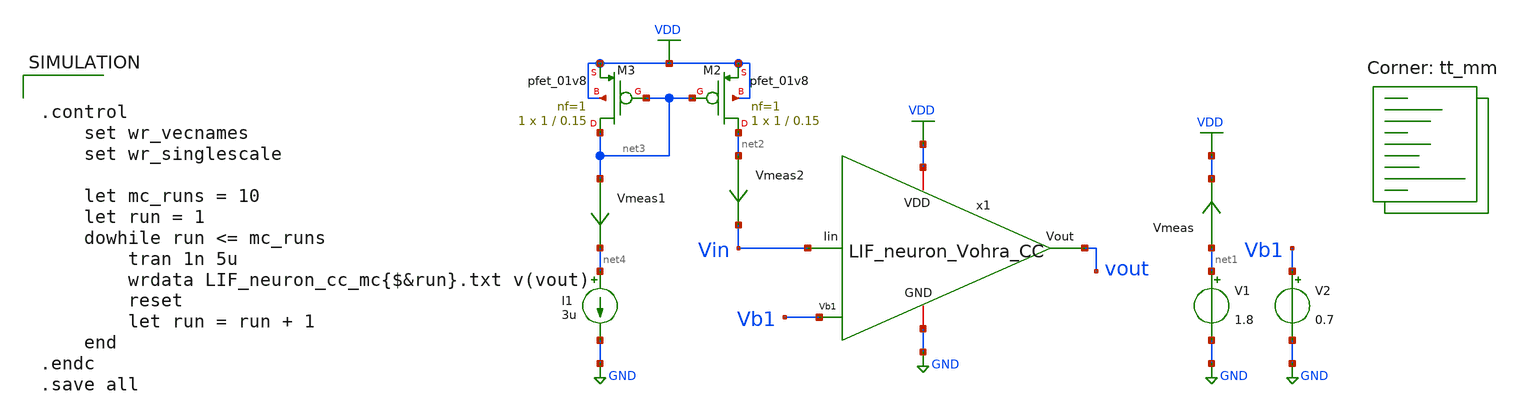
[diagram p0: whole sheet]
** sch_path: LIF_neuron/LIF_neuron_cc_mc.sch
**.subckt LIF_neuron_cc_mc
V1 net1 GND 1.8
V2 Vb1 GND 0.7
x1 VDD vout Vb1 GND Vin LIF_neuron_Vohra_CC
I1 net4 GND 3u
XM2 net2 net3 VDD VDD sky130_fd_pr__pfet_01v8 L=0.15 W=1 nf=1 ad='int((nf+1)/2) * W/nf * 0.29' as='int((nf+2)/2) * W/nf * 0.29'
+ pd='2*int((nf+1)/2) * (W/nf + 0.29)' ps='2*int((nf+2)/2) * (W/nf + 0.29)' nrd='0.29 / W' nrs='0.29 / W'
+ sa=0 sb=0 sd=0 mult=1 m=1
XM3 net3 net3 VDD VDD sky130_fd_pr__pfet_01v8 L=0.15 W=1 nf=1 ad='int((nf+1)/2) * W/nf * 0.29' as='int((nf+2)/2) * W/nf * 0.29'
+ pd='2*int((nf+1)/2) * (W/nf + 0.29)' ps='2*int((nf+2)/2) * (W/nf + 0.29)' nrd='0.29 / W' nrs='0.29 / W'
+ sa=0 sb=0 sd=0 mult=1 m=1
Vmeas net1 VDD 0
.save i(vmeas)
Vmeas1 net3 net4 0
.save i(vmeas1)
Vmeas2 net2 Vin 0
.save i(vmeas2)
**** begin user architecture code


.control
	set wr_vecnames
	set wr_singlescale

	let mc_runs = 10
	let run = 1
	dowhile run <= mc_runs
		tran 1n 5u
		wrdata LIF_neuron_cc_mc{$&run}.txt v(vout)
		reset
		let run = run + 1
	end
.endc
.save all


.lib $::SKYWATER_MODELS/sky130.lib.spice tt_mm
**** end user architecture code
**.ends

* expanding   symbol:  /home/ricardo/RATT_repos/Proyectos_xschem/LIF_neuron/LIF_neuron_Vohra_CC.sym
*+ # of pins=5
** sym_path: LIF_neuron/LIF_neuron_Vohra_CC.sym
** sch_path: LIF_neuron/LIF_neuron_Vohra_CC.sch
.subckt LIF_neuron_Vohra_CC VDD Vout Vb1 GND Iin
*.iopin GND
*.ipin Vb1
*.iopin VDD
*.opin Vout
*.ipin Iin
XM8 net2 Vb1 GND GND sky130_fd_pr__nfet_01v8 L=0.5 W=5 nf=1 ad='int((nf+1)/2) * W/nf * 0.29' as='int((nf+2)/2) * W/nf * 0.29'
+ pd='2*int((nf+1)/2) * (W/nf + 0.29)' ps='2*int((nf+2)/2) * (W/nf + 0.29)' nrd='0.29 / W' nrs='0.29 / W'
+ sa=0 sb=0 sd=0 mult=1 m=1
XM7 rc net1 net2 GND sky130_fd_pr__nfet_01v8 L=1 W=1 nf=1 ad='int((nf+1)/2) * W/nf * 0.29' as='int((nf+2)/2) * W/nf * 0.29'
+ pd='2*int((nf+1)/2) * (W/nf + 0.29)' ps='2*int((nf+2)/2) * (W/nf + 0.29)' nrd='0.29 / W' nrs='0.29 / W'
+ sa=0 sb=0 sd=0 mult=1 m=1
XM6 rc net1 VDD VDD sky130_fd_pr__pfet_01v8 L=1 W=5 nf=1 ad='int((nf+1)/2) * W/nf * 0.29' as='int((nf+2)/2) * W/nf * 0.29'
+ pd='2*int((nf+1)/2) * (W/nf + 0.29)' ps='2*int((nf+2)/2) * (W/nf + 0.29)' nrd='0.29 / W' nrs='0.29 / W'
+ sa=0 sb=0 sd=0 mult=1 m=1
XCr rc GND sky130_fd_pr__cap_mim_m3_1 W=10 L=1 MF=1 m=1
XM9 Iin rc GND GND sky130_fd_pr__nfet_01v8 L=1 W=5 nf=1 ad='int((nf+1)/2) * W/nf * 0.29' as='int((nf+2)/2) * W/nf * 0.29'
+ pd='2*int((nf+1)/2) * (W/nf + 0.29)' ps='2*int((nf+2)/2) * (W/nf + 0.29)' nrd='0.29 / W' nrs='0.29 / W'
+ sa=0 sb=0 sd=0 mult=1 m=1
XCm Iin GND sky130_fd_pr__cap_mim_m3_1 W=30 L=1 MF=50 m=50
XM5 net3 Vout GND GND sky130_fd_pr__nfet_01v8 L=0.5 W=1 nf=1 ad='int((nf+1)/2) * W/nf * 0.29' as='int((nf+2)/2) * W/nf * 0.29'
+ pd='2*int((nf+1)/2) * (W/nf + 0.29)' ps='2*int((nf+2)/2) * (W/nf + 0.29)' nrd='0.29 / W' nrs='0.29 / W'
+ sa=0 sb=0 sd=0 mult=1 m=1
XM3 net1 Iin net3 GND sky130_fd_pr__nfet_01v8 L=1 W=1 nf=1 ad='int((nf+1)/2) * W/nf * 0.29' as='int((nf+2)/2) * W/nf * 0.29'
+ pd='2*int((nf+1)/2) * (W/nf + 0.29)' ps='2*int((nf+2)/2) * (W/nf + 0.29)' nrd='0.29 / W' nrs='0.29 / W'
+ sa=0 sb=0 sd=0 mult=1 m=1
XM1 net1 Iin VDD VDD sky130_fd_pr__pfet_01v8 L=1 W=1 nf=1 ad='int((nf+1)/2) * W/nf * 0.29' as='int((nf+2)/2) * W/nf * 0.29'
+ pd='2*int((nf+1)/2) * (W/nf + 0.29)' ps='2*int((nf+2)/2) * (W/nf + 0.29)' nrd='0.29 / W' nrs='0.29 / W'
+ sa=0 sb=0 sd=0 mult=1 m=1
XM4 Vout net1 net3 GND sky130_fd_pr__nfet_01v8 L=1 W=1 nf=1 ad='int((nf+1)/2) * W/nf * 0.29' as='int((nf+2)/2) * W/nf * 0.29'
+ pd='2*int((nf+1)/2) * (W/nf + 0.29)' ps='2*int((nf+2)/2) * (W/nf + 0.29)' nrd='0.29 / W' nrs='0.29 / W'
+ sa=0 sb=0 sd=0 mult=1 m=1
XM2 Vout net1 VDD VDD sky130_fd_pr__pfet_01v8 L=1 W=5 nf=1 ad='int((nf+1)/2) * W/nf * 0.29' as='int((nf+2)/2) * W/nf * 0.29'
+ pd='2*int((nf+1)/2) * (W/nf + 0.29)' ps='2*int((nf+2)/2) * (W/nf + 0.29)' nrd='0.29 / W' nrs='0.29 / W'
+ sa=0 sb=0 sd=0 mult=1 m=1
.ends

.GLOBAL GND
.GLOBAL VDD
.end
